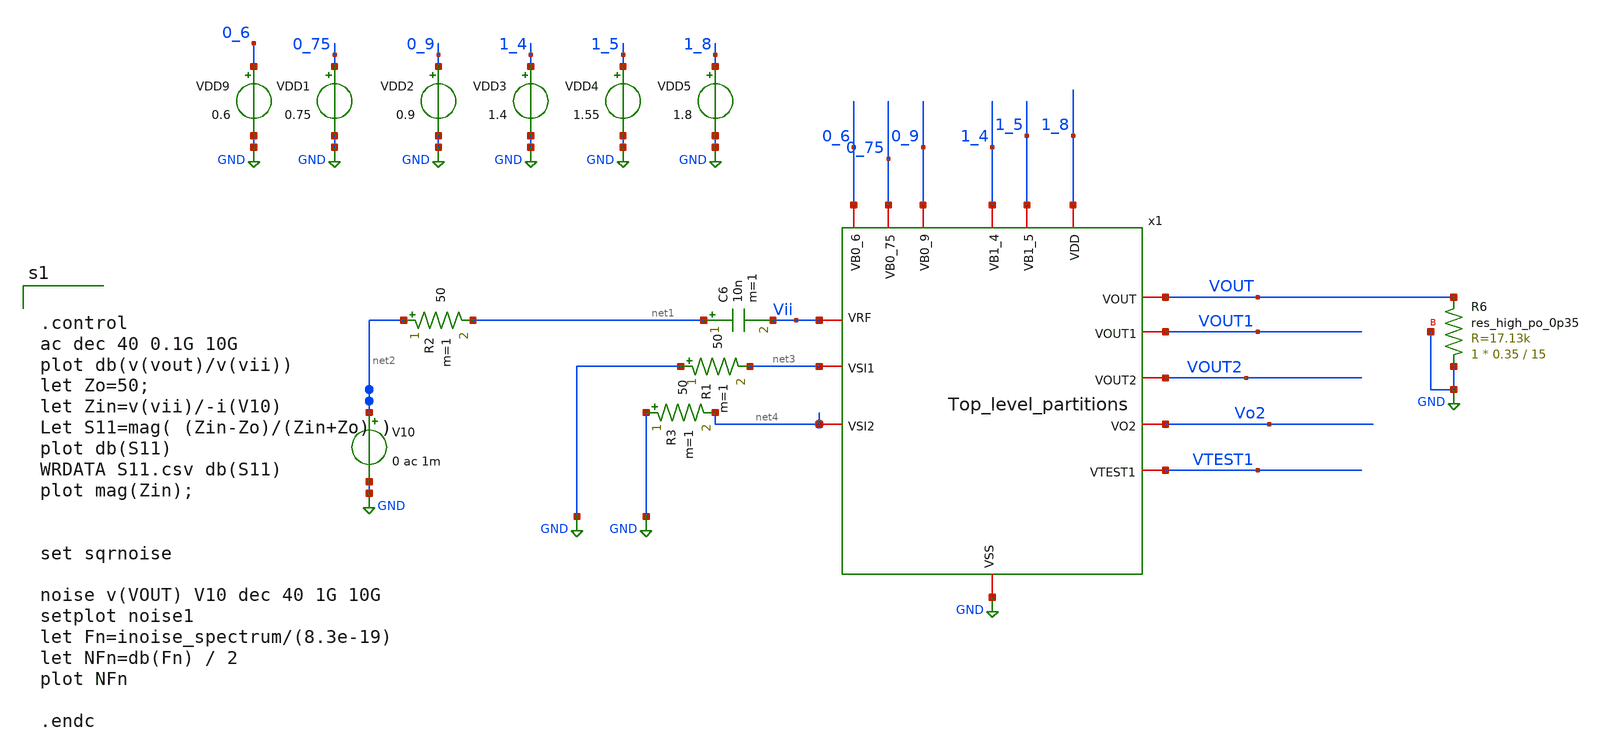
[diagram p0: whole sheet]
** sch_path: xschem/xschem4_sic_oct_20/Top_level_partitions_tb.sch
**.subckt Top_level_partitions_tb
x1 1_5 1_8 VOUT2 VOUT1 0_6 0_75 0_9 VOUT Vii net4 1_4 VTEST1 net3 GND Vo2 Top_level_partitions
VDD9 0_6 GND 0.6
VDD1 0_75 GND 0.75
VDD2 0_9 GND 0.9
VDD3 1_4 GND 1.4
VDD4 1_5 GND 1.55
VDD5 1_8 GND 1.8
C6 net1 Vii 10n m=1
V10 net2 GND 0 ac 1m
R2 net2 net1 50 m=1
XR6 GND VOUT GND sky130_fd_pr__res_high_po_0p35 L=15 mult=1 m=1
R1 GND net3 50 m=1
R3 GND net4 50 m=1
**** begin user architecture code


.control
ac dec 40 0.1G 10G
plot db(v(vout)/v(vii))
let Zo=50;
let Zin=v(vii)/-i(V10)
Let S11=mag( (Zin-Zo)/(Zin+Zo) )
plot db(S11)
WRDATA S11.csv db(S11)
plot mag(Zin);


set sqrnoise

noise v(VOUT) V10 dec 40 1G 10G
setplot noise1
let Fn=inoise_spectrum/(8.3e-19)
let NFn=db(Fn) / 2
plot NFn

.endc



.lib $::SKYWATER_MODELS/sky130.lib.spice tt

**** end user architecture code
**.ends

* expanding   symbol:  Top_level_partitions.sym # of pins=15
** sym_path: xschem/xschem4_sic_oct_20/Top_level_partitions.sym
** sch_path: xschem/xschem4_sic_oct_20/Top_level_partitions.sch
.subckt Top_level_partitions VB1_5 VDD VOUT2 VOUT1 VB0_6 VB0_75 VB0_9 VOUT VRF VSI2 VB1_4 VTEST1
+ VSI1 VSS VO2
*.iopin VDD
*.iopin VSS
*.iopin VB1_5
*.iopin VRF
*.iopin VB1_4
*.iopin VB0_75
*.iopin VSI1
*.iopin VB0_9
*.iopin VB0_6
*.iopin VSI2
*.iopin VOUT
*.iopin VTEST1
*.iopin VOUT2
*.iopin VOUT1
*.iopin VO2
x1 VOUT1 VDD VB1_4 VTEST1 VRF VSI1 VB0_75 VSS partition1
x2 VOUT2 VDD VOUT1 VSS VB1_5 VRF partition2
x3 VDD VOUT2 VO2 VOUT1 VSS VB0_9 partition3
x4 VDD VB0_6 VO2 VSI2 VSS VB0_75 partition4
x5 VDD VO2 VOUT VSS partition5
.ends


* expanding   symbol:  partition1.sym # of pins=8
** sym_path: xschem/xschem4_sic_oct_20/partition1.sym
** sch_path: xschem/xschem4_sic_oct_20/partition1.sch
.subckt partition1 VOUT1 VDD VB1_4 VTEST1 VRF VSI1 VB0_75 VSS
*.iopin VRF
*.iopin VSS
*.iopin VB0_75
*.iopin VSI1
*.iopin VB1_4
*.iopin VTEST1
*.iopin VOUT1
*.iopin VDD
XM12 VTEST1 VRF VSS VSS sky130_fd_pr__nfet_01v8_lvt L=0.15 W=220 nf=22 ad='int((nf+1)/2) * W/nf * 0.29'
+ as='int((nf+2)/2) * W/nf * 0.29' pd='2*int((nf+1)/2) * (W/nf + 0.29)' ps='2*int((nf+2)/2) * (W/nf + 0.29)'
+ nrd='0.29 / W' nrs='0.29 / W' sa=0 sb=0 sd=0 mult=1 m=1
XM13 VTEST1 VRF VDD VDD sky130_fd_pr__pfet_01v8 L=0.15 W=30 nf=3 ad='int((nf+1)/2) * W/nf * 0.29' as='int((nf+2)/2) * W/nf * 0.29'
+ pd='2*int((nf+1)/2) * (W/nf + 0.29)' ps='2*int((nf+2)/2) * (W/nf + 0.29)' nrd='0.29 / W' nrs='0.29 / W'
+ sa=0 sb=0 sd=0 mult=1 m=1
XM14 VOUT1 VB1_4 VTEST1 VSS sky130_fd_pr__nfet_01v8_lvt L=0.15 W=80 nf=8 ad='int((nf+1)/2) * W/nf * 0.29'
+ as='int((nf+2)/2) * W/nf * 0.29' pd='2*int((nf+1)/2) * (W/nf + 0.29)' ps='2*int((nf+2)/2) * (W/nf + 0.29)'
+ nrd='0.29 / W' nrs='0.29 / W' sa=0 sb=0 sd=0 mult=1 m=1
XM16 VRF VB0_75 VSS VSS sky130_fd_pr__nfet_01v8_lvt L=0.15 W=7.8 nf=1 ad='int((nf+1)/2) * W/nf * 0.29'
+ as='int((nf+2)/2) * W/nf * 0.29' pd='2*int((nf+1)/2) * (W/nf + 0.29)' ps='2*int((nf+2)/2) * (W/nf + 0.29)'
+ nrd='0.29 / W' nrs='0.29 / W' sa=0 sb=0 sd=0 mult=1 m=1
XM20 VTEST1 VSI1 VSS VSS sky130_fd_pr__nfet_01v8_lvt L=0.15 W=240 nf=24 ad='int((nf+1)/2) * W/nf * 0.29'
+ as='int((nf+2)/2) * W/nf * 0.29' pd='2*int((nf+1)/2) * (W/nf + 0.29)' ps='2*int((nf+2)/2) * (W/nf + 0.29)'
+ nrd='0.29 / W' nrs='0.29 / W' sa=0 sb=0 sd=0 mult=1 m=1
XR16 VB0_75 VSI1 VSS sky130_fd_pr__res_high_po_0p35 L=6.2 mult=1 m=1
.ends


* expanding   symbol:  partition2.sym # of pins=6
** sym_path: xschem/xschem4_sic_oct_20/partition2.sym
** sch_path: xschem/xschem4_sic_oct_20/partition2.sch
.subckt partition2 VOUT2 VDD VOUT1 VSS VB1_5 VRF
*.iopin VDD
*.iopin VOUT1
*.iopin VOUT2
*.iopin VB1_5
*.iopin VSS
*.iopin VRF
XR4 VB1_5 net1 VSS sky130_fd_pr__res_high_po_0p35 L=4 mult=1 m=1
XC5 net1 VOUT1 sky130_fd_pr__cap_mim_m3_2 W=30 L=30 MF=1 m=1
XM15 net2 net1 VRF VSS sky130_fd_pr__nfet_01v8_lvt L=0.15 W=7.8 nf=1 ad='int((nf+1)/2) * W/nf * 0.29'
+ as='int((nf+2)/2) * W/nf * 0.29' pd='2*int((nf+1)/2) * (W/nf + 0.29)' ps='2*int((nf+2)/2) * (W/nf + 0.29)'
+ nrd='0.29 / W' nrs='0.29 / W' sa=0 sb=0 sd=0 mult=1 m=1
XR14 net2 VDD VSS sky130_fd_pr__res_high_po_0p35 L=0.5 mult=1 m=1
XR15 VOUT1 VDD VSS sky130_fd_pr__res_high_po_0p69 L=0.69 mult=8 m=8
XM21 VOUT2 VOUT1 VSS VSS sky130_fd_pr__nfet_01v8_lvt L=0.15 W=7.8 nf=1 ad='int((nf+1)/2) * W/nf * 0.29'
+ as='int((nf+2)/2) * W/nf * 0.29' pd='2*int((nf+1)/2) * (W/nf + 0.29)' ps='2*int((nf+2)/2) * (W/nf + 0.29)'
+ nrd='0.29 / W' nrs='0.29 / W' sa=0 sb=0 sd=0 mult=1 m=1
XR17 VOUT2 VDD VSS sky130_fd_pr__res_high_po_0p35 L=0.5 mult=1 m=1
.ends


* expanding   symbol:  partition3.sym # of pins=6
** sym_path: xschem/xschem4_sic_oct_20/partition3.sym
** sch_path: xschem/xschem4_sic_oct_20/partition3.sch
.subckt partition3 VDD VOUT2 Vo2 VOUT1 VSS VB0_9
*.iopin VB0_9
*.iopin VDD
*.iopin VSS
*.iopin VOUT2
*.iopin VOUT1
*.iopin Vo2
XM17 Vo2 net2 VSS VSS sky130_fd_pr__nfet_01v8_lvt L=0.15 W=45 nf=7 ad='int((nf+1)/2) * W/nf * 0.29' as='int((nf+2)/2) * W/nf * 0.29'
+ pd='2*int((nf+1)/2) * (W/nf + 0.29)' ps='2*int((nf+2)/2) * (W/nf + 0.29)' nrd='0.29 / W' nrs='0.29 / W'
+ sa=0 sb=0 sd=0 mult=1 m=1
XM18 VDD net1 Vo2 VSS sky130_fd_pr__nfet_01v8_lvt L=0.15 W=12 nf=3 ad='int((nf+1)/2) * W/nf * 0.29' as='int((nf+2)/2) * W/nf * 0.29'
+ pd='2*int((nf+1)/2) * (W/nf + 0.29)' ps='2*int((nf+2)/2) * (W/nf + 0.29)' nrd='0.29 / W' nrs='0.29 / W'
+ sa=0 sb=0 sd=0 mult=1 m=1
XR11 net1 VDD VSS sky130_fd_pr__res_high_po_0p35 L=15 mult=1 m=1
XC7 VOUT2 net1 sky130_fd_pr__cap_mim_m3_2 W=30 L=30 MF=1 m=1
XR12 VB0_9 net2 VSS sky130_fd_pr__res_high_po_0p35 L=8 mult=1 m=1
XC8 VOUT1 net2 sky130_fd_pr__cap_mim_m3_2 W=30 L=30 MF=1 m=1
XD1 VSS net1 sky130_fd_pr__diode_pw2nd_05v5 area=1e12 pj=4e6
.ends


* expanding   symbol:  partition4.sym # of pins=6
** sym_path: xschem/xschem4_sic_oct_20/partition4.sym
** sch_path: xschem/xschem4_sic_oct_20/partition4.sch
.subckt partition4 VDD VB0_6 V02 VSI2 VSS VB0_75
*.iopin VSI2
*.iopin VB0_6
*.iopin VDD
*.iopin VSS
*.iopin VB0_75
*.iopin V02
XM19 V02 net1 VDD VDD sky130_fd_pr__pfet_01v8 L=0.15 W=30 nf=3 ad='int((nf+1)/2) * W/nf * 0.29' as='int((nf+2)/2) * W/nf * 0.29'
+ pd='2*int((nf+1)/2) * (W/nf + 0.29)' ps='2*int((nf+2)/2) * (W/nf + 0.29)' nrd='0.29 / W' nrs='0.29 / W'
+ sa=0 sb=0 sd=0 mult=1 m=1
XR13 VB0_6 net1 VSS sky130_fd_pr__res_high_po_0p35 L=6.2 mult=1 m=1
XM22 V02 VSI2 VSS VSS sky130_fd_pr__nfet_01v8_lvt L=0.15 W=80 nf=8 ad='int((nf+1)/2) * W/nf * 0.29' as='int((nf+2)/2) * W/nf * 0.29'
+ pd='2*int((nf+1)/2) * (W/nf + 0.29)' ps='2*int((nf+2)/2) * (W/nf + 0.29)' nrd='0.29 / W' nrs='0.29 / W'
+ sa=0 sb=0 sd=0 mult=1 m=1
XR18 VB0_75 VSI2 VSS sky130_fd_pr__res_high_po_0p35 L=0.5 mult=1 m=1
.ends


* expanding   symbol:  partition5.sym # of pins=4
** sym_path: xschem/xschem4_sic_oct_20/partition5.sym
** sch_path: xschem/xschem4_sic_oct_20/partition5.sch
.subckt partition5 VDD VO2 VOUT VSS
*.iopin VOUT
*.iopin VDD
*.iopin VSS
*.iopin VO2
XM4 VDD net1 VOUT VSS sky130_fd_pr__nfet_01v8_lvt L=0.15 W=100 nf=10 ad='int((nf+1)/2) * W/nf * 0.29'
+ as='int((nf+2)/2) * W/nf * 0.29' pd='2*int((nf+1)/2) * (W/nf + 0.29)' ps='2*int((nf+2)/2) * (W/nf + 0.29)'
+ nrd='0.29 / W' nrs='0.29 / W' sa=0 sb=0 sd=0 mult=1 m=1
XR5 net1 VDD VSS sky130_fd_pr__res_high_po_0p35 L=4 mult=1 m=1
XR6 VSS VOUT VSS sky130_fd_pr__res_high_po_0p35 L=15 mult=1 m=1
XC3 VO2 net1 sky130_fd_pr__cap_mim_m3_2 W=30 L=30 MF=1 m=1
.ends

.GLOBAL GND
.end
